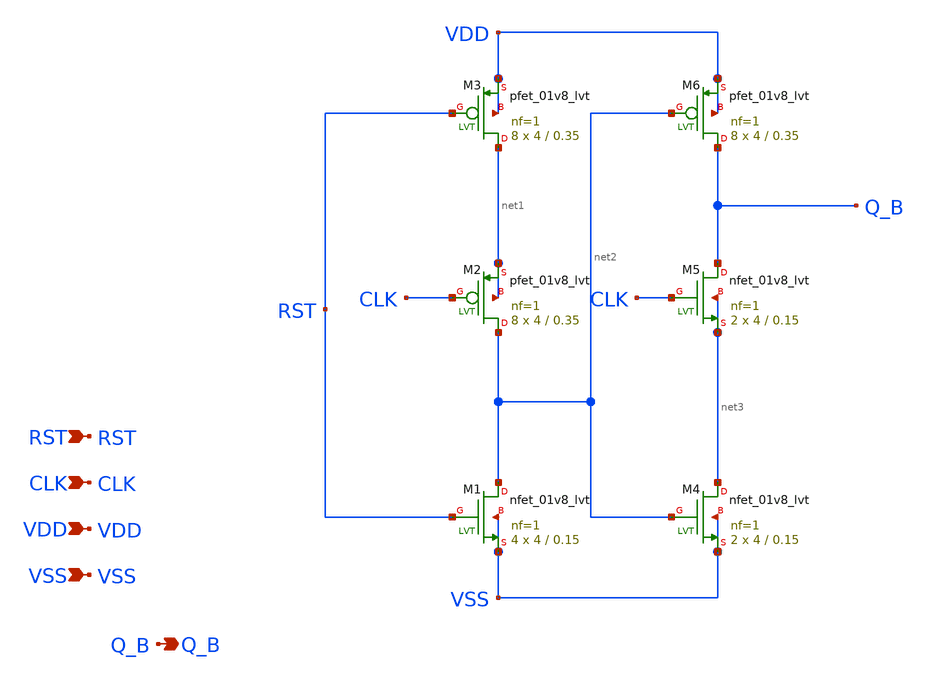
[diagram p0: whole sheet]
** sch_path: design/LELO_SVOD_SKY130A/LELO_TSPC.sch
**.subckt LELO_TSPC RST CLK VDD VSS Q_B
*.ipin RST
*.ipin CLK
*.ipin VDD
*.ipin VSS
*.opin Q_B
XM1 net2 RST VSS VSS sky130_fd_pr__nfet_01v8_lvt L=0.15 W=4 nf=1 ad='int((1 + 1)/2) * 4 / 1 * 0.29' as='int((1 + 2)/2) * 4 / 1 * 0.29'
+ pd='2*int((1 + 1)/2) * (4 / 1 + 0.29)' ps='2*int((1 + 2)/2) * (4 / 1 + 0.29)' nrd='0.29 / 4 ' nrs='0.29 / 4 '
+ sa=0 sb=0 sd=0 mult=4 m=4
XM2 net2 CLK net1 net1 sky130_fd_pr__pfet_01v8_lvt L=0.35 W=4 nf=1 ad='int((1 + 1)/2) * 4 / 1 * 0.29'
+ as='int((1 + 2)/2) * 4 / 1 * 0.29' pd='2*int((1 + 1)/2) * (4 / 1 + 0.29)' ps='2*int((1 + 2)/2) * (4 / 1 + 0.29)'
+ nrd='0.29 / 4 ' nrs='0.29 / 4 ' sa=0 sb=0 sd=0 mult=8 m=8
XM3 net1 RST VDD VDD sky130_fd_pr__pfet_01v8_lvt L=0.35 W=4 nf=1 ad='int((1 + 1)/2) * 4 / 1 * 0.29' as='int((1 + 2)/2) * 4 / 1 * 0.29'
+ pd='2*int((1 + 1)/2) * (4 / 1 + 0.29)' ps='2*int((1 + 2)/2) * (4 / 1 + 0.29)' nrd='0.29 / 4 ' nrs='0.29 / 4 '
+ sa=0 sb=0 sd=0 mult=8 m=8
XM4 net3 net2 VSS VSS sky130_fd_pr__nfet_01v8_lvt L=0.15 W=4 nf=1 ad='int((1 + 1)/2) * 4 / 1 * 0.29'
+ as='int((1 + 2)/2) * 4 / 1 * 0.29' pd='2*int((1 + 1)/2) * (4 / 1 + 0.29)' ps='2*int((1 + 2)/2) * (4 / 1 + 0.29)'
+ nrd='0.29 / 4 ' nrs='0.29 / 4 ' sa=0 sb=0 sd=0 mult=2 m=2
XM5 Q_B CLK net3 net3 sky130_fd_pr__nfet_01v8_lvt L=0.15 W=4 nf=1 ad='int((1 + 1)/2) * 4 / 1 * 0.29'
+ as='int((1 + 2)/2) * 4 / 1 * 0.29' pd='2*int((1 + 1)/2) * (4 / 1 + 0.29)' ps='2*int((1 + 2)/2) * (4 / 1 + 0.29)'
+ nrd='0.29 / 4 ' nrs='0.29 / 4 ' sa=0 sb=0 sd=0 mult=2 m=2
XM6 Q_B net2 VDD VDD sky130_fd_pr__pfet_01v8_lvt L=0.35 W=4 nf=1 ad='int((1 + 1)/2) * 4 / 1 * 0.29' as='int((1 + 2)/2) * 4 / 1 * 0.29'
+ pd='2*int((1 + 1)/2) * (4 / 1 + 0.29)' ps='2*int((1 + 2)/2) * (4 / 1 + 0.29)' nrd='0.29 / 4 ' nrs='0.29 / 4 '
+ sa=0 sb=0 sd=0 mult=8 m=8
**.ends
.end
